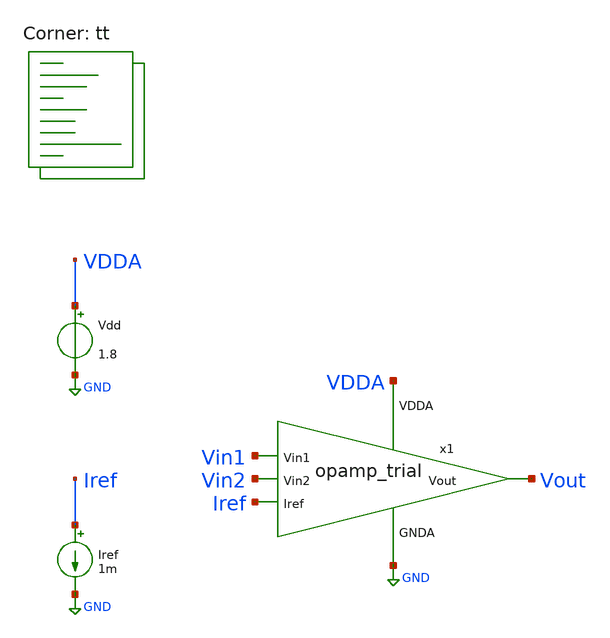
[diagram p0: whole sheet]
** sch_path: projects/pll/trials/tb_opamp_trial.sch
**.subckt tb_opamp_trial
x1 VDDA Vin1 Vin2 Iref Vout GND opamp_trial
Vdd VDDA GND 1.8
Iref Iref GND 1m
**** begin user architecture code

blabla

.lib $::SKYWATER_MODELS/sky130.lib.spice tt
**** end user architecture code
**.ends

* expanding   symbol:  /foss/designs/my_design/projects/pll/trials/opamp_trial.sym # of pins=6
** sym_path: projects/pll/trials/opamp_trial.sym
** sch_path: projects/pll/trials/opamp_trial.sch
.subckt opamp_trial VDDA Vin1 Vin2 Iref Vout GNDA
*.ipin Vin1
*.ipin Vin2
*.ipin Iref
*.opin Vout
*.ipin VDDA
*.ipin GNDA
XM1 net2 net1 GNDA GNDA sky130_fd_pr__nfet_01v8 L=0.15 W=1 nf=1 ad='int((nf+1)/2) * W/nf * 0.29' as='int((nf+2)/2) * W/nf * 0.29'
+ pd='2*int((nf+1)/2) * (W/nf + 0.29)' ps='2*int((nf+2)/2) * (W/nf + 0.29)' nrd='0.29 / W' nrs='0.29 / W'
+ sa=0 sb=0 sd=0 mult=1 m=1
XM2 net2 Vin2 net3 VDDA sky130_fd_pr__pfet_01v8 L=0.15 W=2 nf=1 ad='int((nf+1)/2) * W/nf * 0.29' as='int((nf+2)/2) * W/nf * 0.29'
+ pd='2*int((nf+1)/2) * (W/nf + 0.29)' ps='2*int((nf+2)/2) * (W/nf + 0.29)' nrd='0.29 / W' nrs='0.29 / W'
+ sa=0 sb=0 sd=0 mult=1 m=1
XM3 net1 net1 GNDA GNDA sky130_fd_pr__nfet_01v8 L=0.15 W=1 nf=1 ad='int((nf+1)/2) * W/nf * 0.29' as='int((nf+2)/2) * W/nf * 0.29'
+ pd='2*int((nf+1)/2) * (W/nf + 0.29)' ps='2*int((nf+2)/2) * (W/nf + 0.29)' nrd='0.29 / W' nrs='0.29 / W'
+ sa=0 sb=0 sd=0 mult=1 m=1
XM4 net1 Vin1 net3 VDDA sky130_fd_pr__pfet_01v8 L=0.15 W=2 nf=1 ad='int((nf+1)/2) * W/nf * 0.29' as='int((nf+2)/2) * W/nf * 0.29'
+ pd='2*int((nf+1)/2) * (W/nf + 0.29)' ps='2*int((nf+2)/2) * (W/nf + 0.29)' nrd='0.29 / W' nrs='0.29 / W'
+ sa=0 sb=0 sd=0 mult=1 m=1
XM5 net3 Iref VDDA VDDA sky130_fd_pr__pfet_01v8 L=0.15 W=4 nf=1 ad='int((nf+1)/2) * W/nf * 0.29' as='int((nf+2)/2) * W/nf * 0.29'
+ pd='2*int((nf+1)/2) * (W/nf + 0.29)' ps='2*int((nf+2)/2) * (W/nf + 0.29)' nrd='0.29 / W' nrs='0.29 / W'
+ sa=0 sb=0 sd=0 mult=1 m=1
XM6 Vout Iref VDDA VDDA sky130_fd_pr__pfet_01v8 L=0.15 W=8 nf=1 ad='int((nf+1)/2) * W/nf * 0.29' as='int((nf+2)/2) * W/nf * 0.29'
+ pd='2*int((nf+1)/2) * (W/nf + 0.29)' ps='2*int((nf+2)/2) * (W/nf + 0.29)' nrd='0.29 / W' nrs='0.29 / W'
+ sa=0 sb=0 sd=0 mult=1 m=1
XM7 Vout net2 GNDA GNDA sky130_fd_pr__nfet_01v8 L=0.15 W=4 nf=1 ad='int((nf+1)/2) * W/nf * 0.29' as='int((nf+2)/2) * W/nf * 0.29'
+ pd='2*int((nf+1)/2) * (W/nf + 0.29)' ps='2*int((nf+2)/2) * (W/nf + 0.29)' nrd='0.29 / W' nrs='0.29 / W'
+ sa=0 sb=0 sd=0 mult=1 m=1
XM8 Iref Iref VDDA VDDA sky130_fd_pr__pfet_01v8 L=0.15 W=2 nf=1 ad='int((nf+1)/2) * W/nf * 0.29' as='int((nf+2)/2) * W/nf * 0.29'
+ pd='2*int((nf+1)/2) * (W/nf + 0.29)' ps='2*int((nf+2)/2) * (W/nf + 0.29)' nrd='0.29 / W' nrs='0.29 / W'
+ sa=0 sb=0 sd=0 mult=1 m=1
.ends

.GLOBAL GND
.end
